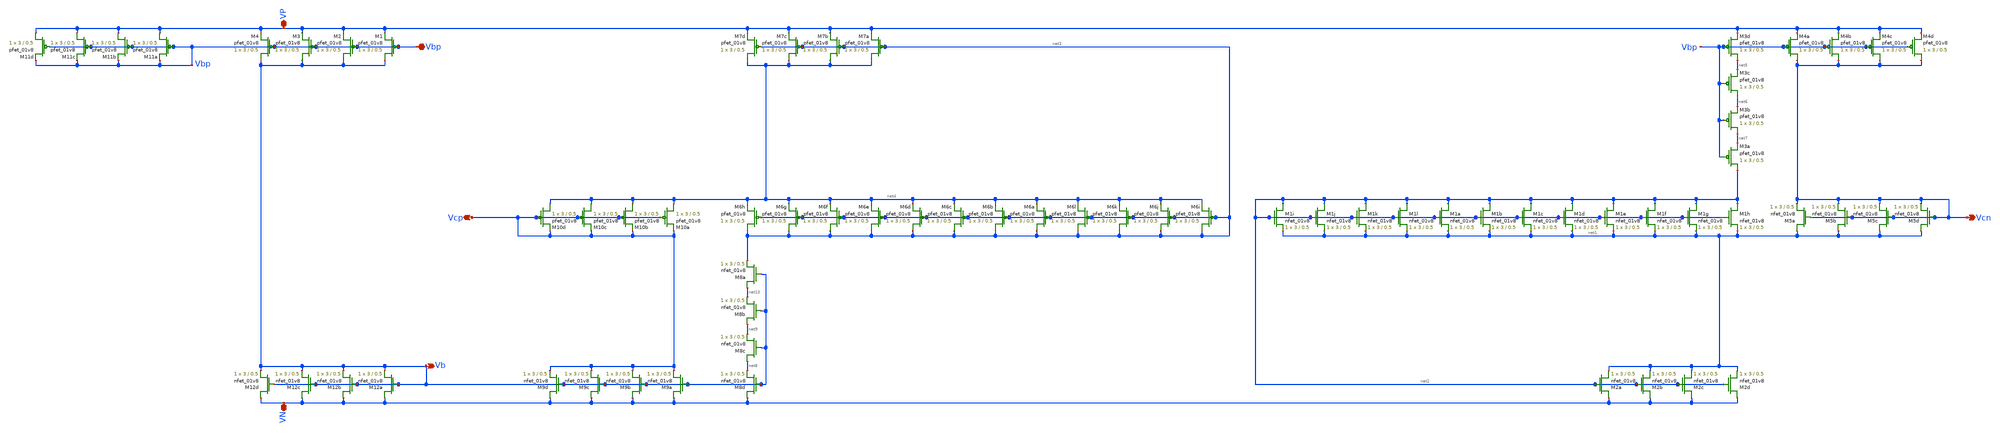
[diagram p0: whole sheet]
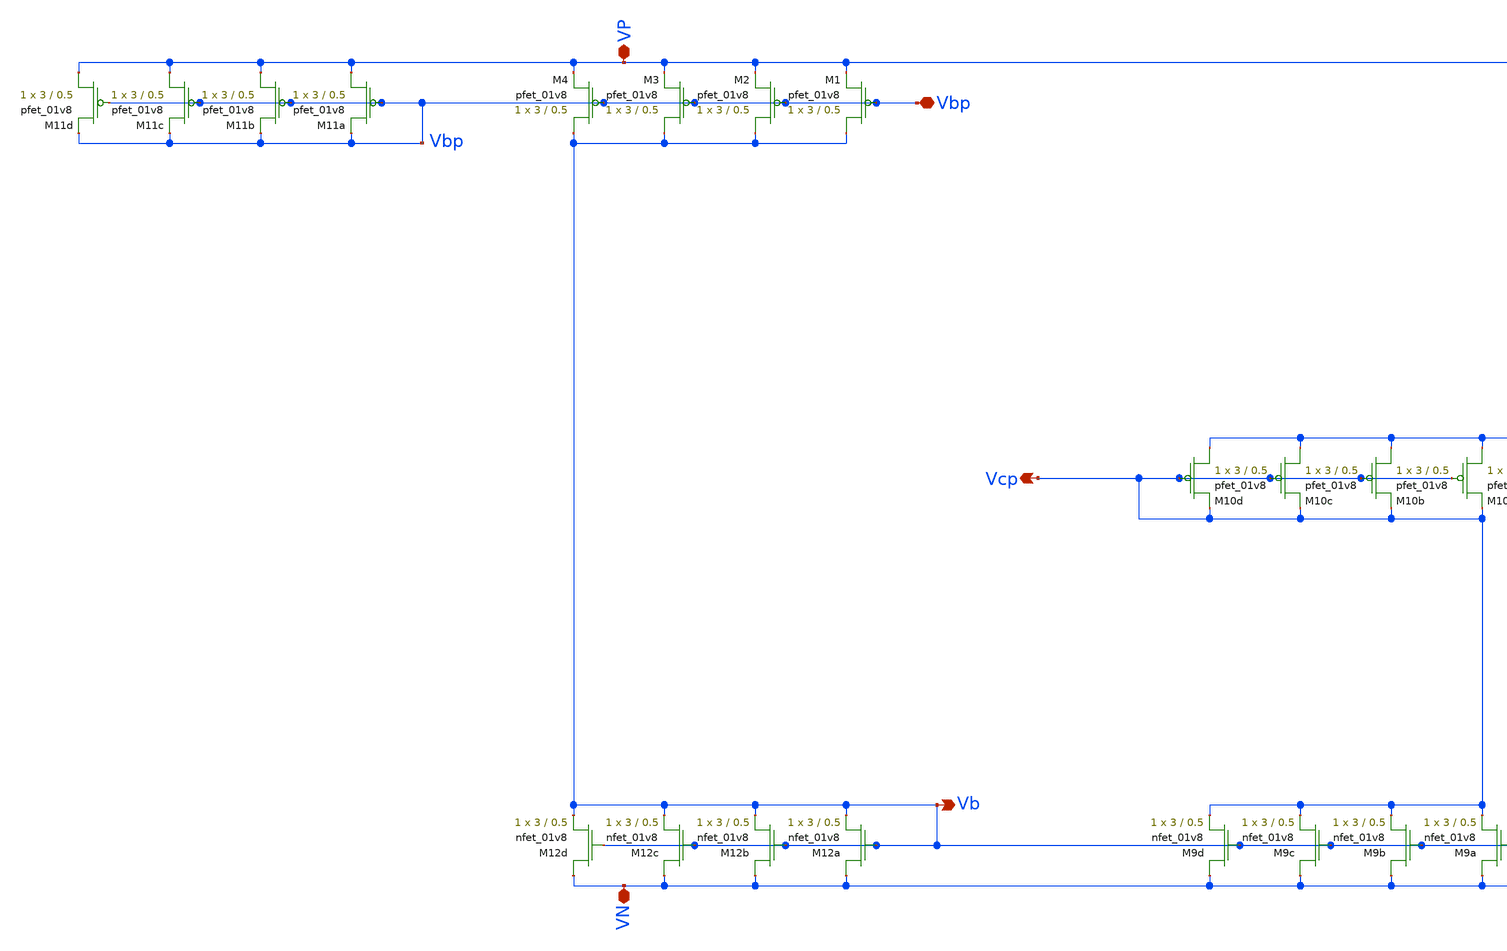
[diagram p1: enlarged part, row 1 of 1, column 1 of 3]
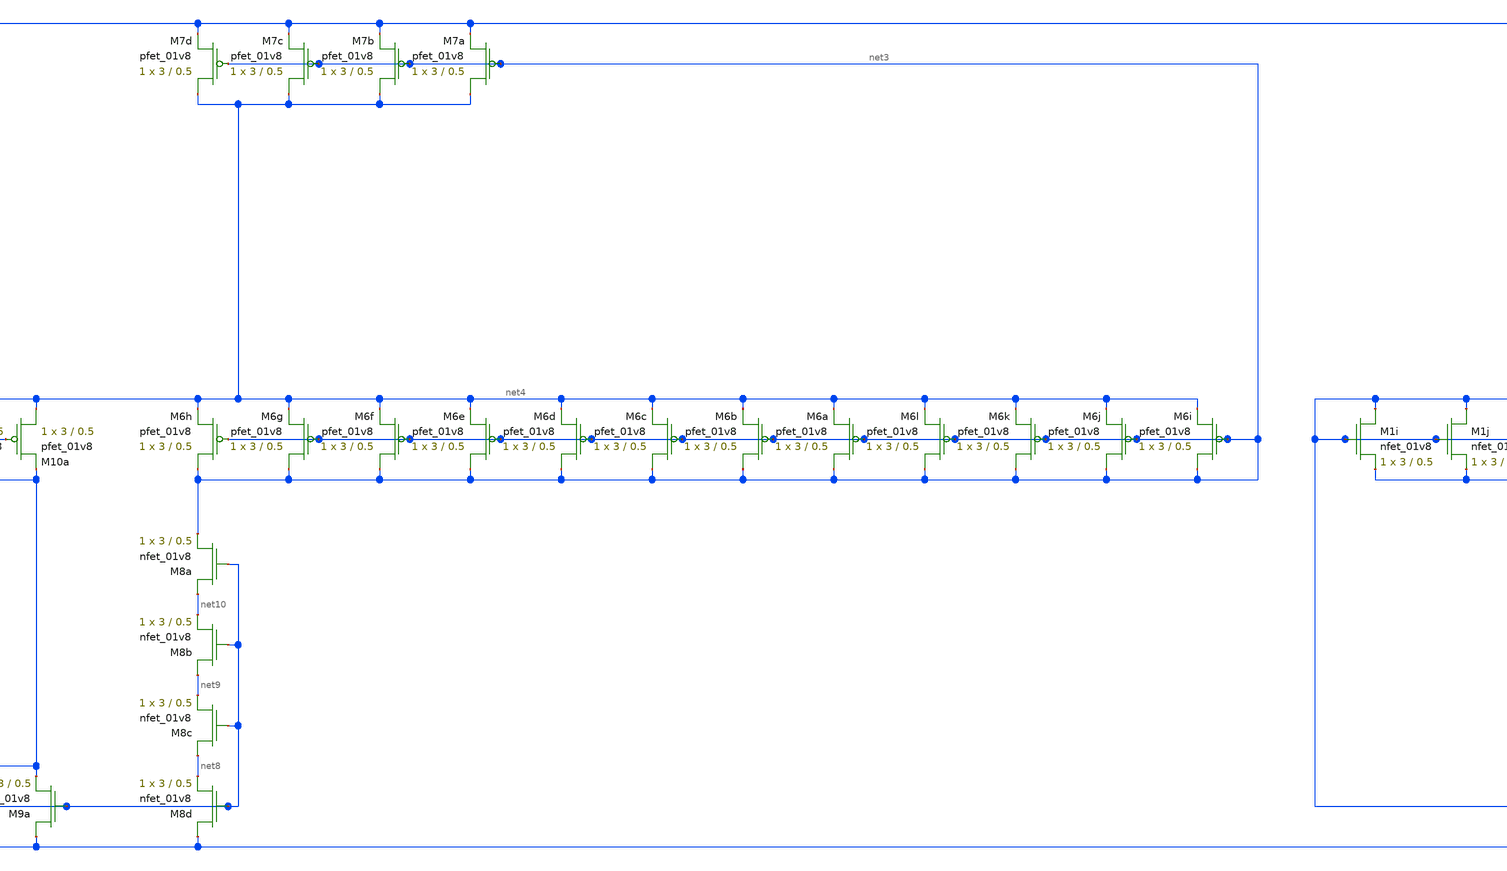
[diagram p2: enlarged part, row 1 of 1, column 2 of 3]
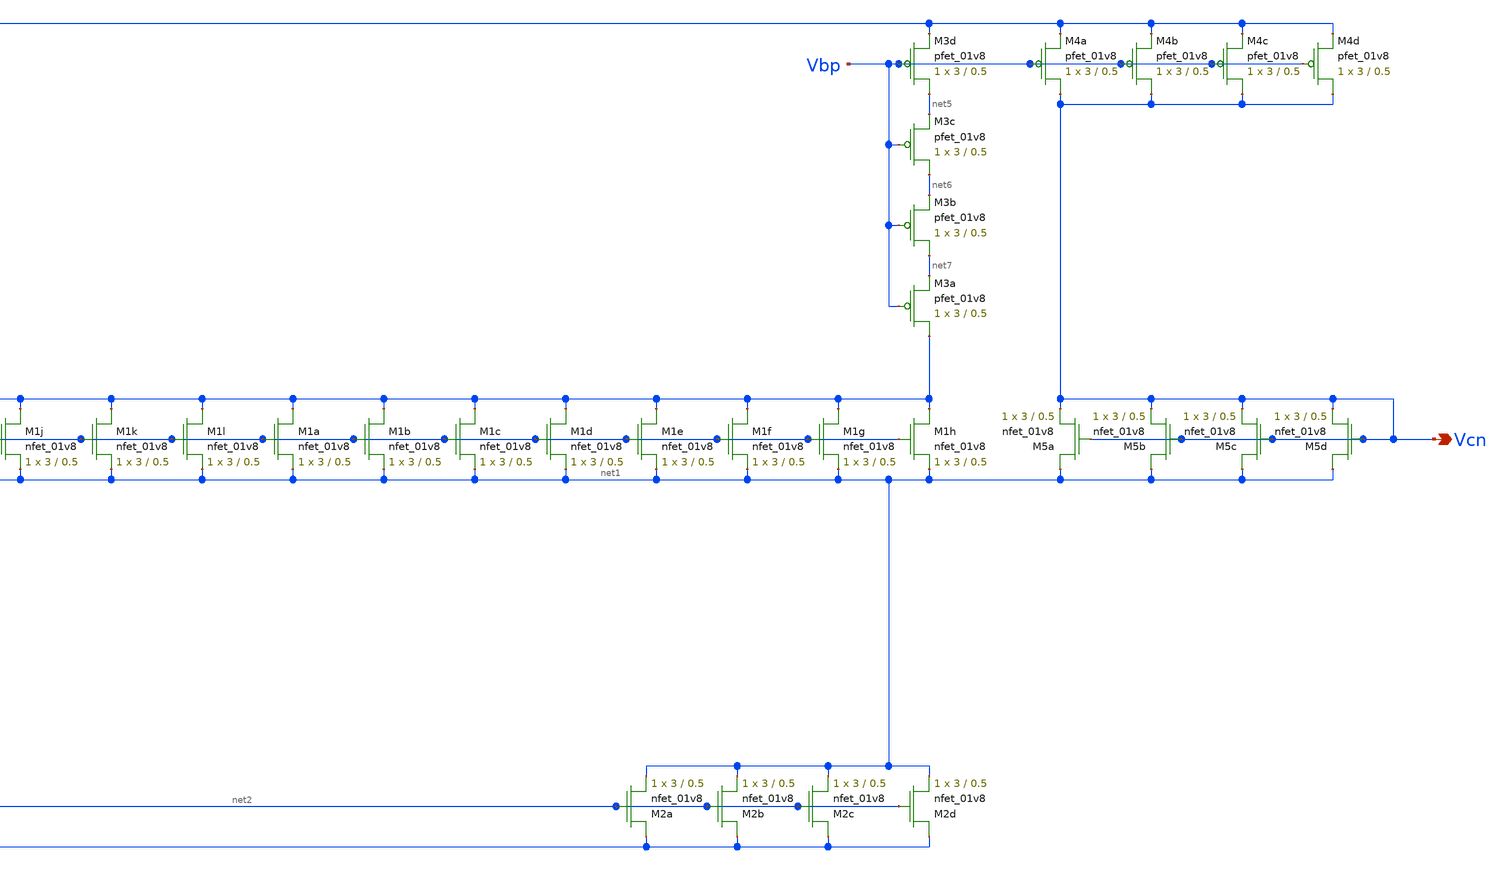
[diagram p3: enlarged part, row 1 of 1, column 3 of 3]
** sch_path: xschem/other_project_files/bias_schematic.sch
**.subckt bias_schematic VP VN Vcp Vbp Vcn Vb
*.iopin VP
*.iopin VN
*.opin Vcp
*.iopin Vbp
*.opin Vcn
*.opin Vb
XM1a net2 net2 net1 GND sky130_fd_pr__nfet_01v8 L=0.5 W=3 nf=1 ad='int((nf+1)/2) * W/nf * 0.29' as='int((nf+2)/2) * W/nf * 0.29'
+ pd='2*int((nf+1)/2) * (W/nf + 0.29)' ps='2*int((nf+2)/2) * (W/nf + 0.29)' nrd='0.29 / W' nrs='0.29 / W'
+ sa=0 sb=0 sd=0 mult=1 m=1
XM1b net2 net2 net1 GND sky130_fd_pr__nfet_01v8 L=0.5 W=3 nf=1 ad='int((nf+1)/2) * W/nf * 0.29' as='int((nf+2)/2) * W/nf * 0.29'
+ pd='2*int((nf+1)/2) * (W/nf + 0.29)' ps='2*int((nf+2)/2) * (W/nf + 0.29)' nrd='0.29 / W' nrs='0.29 / W'
+ sa=0 sb=0 sd=0 mult=1 m=1
XM1c net2 net2 net1 GND sky130_fd_pr__nfet_01v8 L=0.5 W=3 nf=1 ad='int((nf+1)/2) * W/nf * 0.29' as='int((nf+2)/2) * W/nf * 0.29'
+ pd='2*int((nf+1)/2) * (W/nf + 0.29)' ps='2*int((nf+2)/2) * (W/nf + 0.29)' nrd='0.29 / W' nrs='0.29 / W'
+ sa=0 sb=0 sd=0 mult=1 m=1
XM1d net2 net2 net1 GND sky130_fd_pr__nfet_01v8 L=0.5 W=3 nf=1 ad='int((nf+1)/2) * W/nf * 0.29' as='int((nf+2)/2) * W/nf * 0.29'
+ pd='2*int((nf+1)/2) * (W/nf + 0.29)' ps='2*int((nf+2)/2) * (W/nf + 0.29)' nrd='0.29 / W' nrs='0.29 / W'
+ sa=0 sb=0 sd=0 mult=1 m=1
XM2a VN net2 net1 GND sky130_fd_pr__nfet_01v8 L=0.5 W=3 nf=1 ad='int((nf+1)/2) * W/nf * 0.29' as='int((nf+2)/2) * W/nf * 0.29'
+ pd='2*int((nf+1)/2) * (W/nf + 0.29)' ps='2*int((nf+2)/2) * (W/nf + 0.29)' nrd='0.29 / W' nrs='0.29 / W'
+ sa=0 sb=0 sd=0 mult=1 m=1
XM2b VN net2 net1 GND sky130_fd_pr__nfet_01v8 L=0.5 W=3 nf=1 ad='int((nf+1)/2) * W/nf * 0.29' as='int((nf+2)/2) * W/nf * 0.29'
+ pd='2*int((nf+1)/2) * (W/nf + 0.29)' ps='2*int((nf+2)/2) * (W/nf + 0.29)' nrd='0.29 / W' nrs='0.29 / W'
+ sa=0 sb=0 sd=0 mult=1 m=1
XM2c VN net2 net1 GND sky130_fd_pr__nfet_01v8 L=0.5 W=3 nf=1 ad='int((nf+1)/2) * W/nf * 0.29' as='int((nf+2)/2) * W/nf * 0.29'
+ pd='2*int((nf+1)/2) * (W/nf + 0.29)' ps='2*int((nf+2)/2) * (W/nf + 0.29)' nrd='0.29 / W' nrs='0.29 / W'
+ sa=0 sb=0 sd=0 mult=1 m=1
XM2d VN net2 net1 GND sky130_fd_pr__nfet_01v8 L=0.5 W=3 nf=1 ad='int((nf+1)/2) * W/nf * 0.29' as='int((nf+2)/2) * W/nf * 0.29'
+ pd='2*int((nf+1)/2) * (W/nf + 0.29)' ps='2*int((nf+2)/2) * (W/nf + 0.29)' nrd='0.29 / W' nrs='0.29 / W'
+ sa=0 sb=0 sd=0 mult=1 m=1
XM3a net2 Vbp net7 VDD sky130_fd_pr__pfet_01v8 L=0.5 W=3 nf=1 ad='int((nf+1)/2) * W/nf * 0.29' as='int((nf+2)/2) * W/nf * 0.29'
+ pd='2*int((nf+1)/2) * (W/nf + 0.29)' ps='2*int((nf+2)/2) * (W/nf + 0.29)' nrd='0.29 / W' nrs='0.29 / W'
+ sa=0 sb=0 sd=0 mult=1 m=1
XM3b net7 Vbp net6 VDD sky130_fd_pr__pfet_01v8 L=0.5 W=3 nf=1 ad='int((nf+1)/2) * W/nf * 0.29' as='int((nf+2)/2) * W/nf * 0.29'
+ pd='2*int((nf+1)/2) * (W/nf + 0.29)' ps='2*int((nf+2)/2) * (W/nf + 0.29)' nrd='0.29 / W' nrs='0.29 / W'
+ sa=0 sb=0 sd=0 mult=1 m=1
XM3c net6 Vbp net5 VDD sky130_fd_pr__pfet_01v8 L=0.5 W=3 nf=1 ad='int((nf+1)/2) * W/nf * 0.29' as='int((nf+2)/2) * W/nf * 0.29'
+ pd='2*int((nf+1)/2) * (W/nf + 0.29)' ps='2*int((nf+2)/2) * (W/nf + 0.29)' nrd='0.29 / W' nrs='0.29 / W'
+ sa=0 sb=0 sd=0 mult=1 m=1
XM3d net5 Vbp VP VDD sky130_fd_pr__pfet_01v8 L=0.5 W=3 nf=1 ad='int((nf+1)/2) * W/nf * 0.29' as='int((nf+2)/2) * W/nf * 0.29'
+ pd='2*int((nf+1)/2) * (W/nf + 0.29)' ps='2*int((nf+2)/2) * (W/nf + 0.29)' nrd='0.29 / W' nrs='0.29 / W'
+ sa=0 sb=0 sd=0 mult=1 m=1
XM4a Vcn Vbp VP VDD sky130_fd_pr__pfet_01v8 L=0.5 W=3 nf=1 ad='int((nf+1)/2) * W/nf * 0.29' as='int((nf+2)/2) * W/nf * 0.29'
+ pd='2*int((nf+1)/2) * (W/nf + 0.29)' ps='2*int((nf+2)/2) * (W/nf + 0.29)' nrd='0.29 / W' nrs='0.29 / W'
+ sa=0 sb=0 sd=0 mult=1 m=1
XM4b Vcn Vbp VP VDD sky130_fd_pr__pfet_01v8 L=0.5 W=3 nf=1 ad='int((nf+1)/2) * W/nf * 0.29' as='int((nf+2)/2) * W/nf * 0.29'
+ pd='2*int((nf+1)/2) * (W/nf + 0.29)' ps='2*int((nf+2)/2) * (W/nf + 0.29)' nrd='0.29 / W' nrs='0.29 / W'
+ sa=0 sb=0 sd=0 mult=1 m=1
XM4c Vcn Vbp VP VDD sky130_fd_pr__pfet_01v8 L=0.5 W=3 nf=1 ad='int((nf+1)/2) * W/nf * 0.29' as='int((nf+2)/2) * W/nf * 0.29'
+ pd='2*int((nf+1)/2) * (W/nf + 0.29)' ps='2*int((nf+2)/2) * (W/nf + 0.29)' nrd='0.29 / W' nrs='0.29 / W'
+ sa=0 sb=0 sd=0 mult=1 m=1
XM4d Vcn Vbp VP VDD sky130_fd_pr__pfet_01v8 L=0.5 W=3 nf=1 ad='int((nf+1)/2) * W/nf * 0.29' as='int((nf+2)/2) * W/nf * 0.29'
+ pd='2*int((nf+1)/2) * (W/nf + 0.29)' ps='2*int((nf+2)/2) * (W/nf + 0.29)' nrd='0.29 / W' nrs='0.29 / W'
+ sa=0 sb=0 sd=0 mult=1 m=1
XM11a VP Vbp Vbp VDD sky130_fd_pr__pfet_01v8 L=0.5 W=3 nf=1 ad='int((nf+1)/2) * W/nf * 0.29' as='int((nf+2)/2) * W/nf * 0.29'
+ pd='2*int((nf+1)/2) * (W/nf + 0.29)' ps='2*int((nf+2)/2) * (W/nf + 0.29)' nrd='0.29 / W' nrs='0.29 / W'
+ sa=0 sb=0 sd=0 mult=1 m=1
XM11b VP Vbp Vbp VDD sky130_fd_pr__pfet_01v8 L=0.5 W=3 nf=1 ad='int((nf+1)/2) * W/nf * 0.29' as='int((nf+2)/2) * W/nf * 0.29'
+ pd='2*int((nf+1)/2) * (W/nf + 0.29)' ps='2*int((nf+2)/2) * (W/nf + 0.29)' nrd='0.29 / W' nrs='0.29 / W'
+ sa=0 sb=0 sd=0 mult=1 m=1
XM11c VP Vbp Vbp VDD sky130_fd_pr__pfet_01v8 L=0.5 W=3 nf=1 ad='int((nf+1)/2) * W/nf * 0.29' as='int((nf+2)/2) * W/nf * 0.29'
+ pd='2*int((nf+1)/2) * (W/nf + 0.29)' ps='2*int((nf+2)/2) * (W/nf + 0.29)' nrd='0.29 / W' nrs='0.29 / W'
+ sa=0 sb=0 sd=0 mult=1 m=1
XM11d VP Vbp Vbp VDD sky130_fd_pr__pfet_01v8 L=0.5 W=3 nf=1 ad='int((nf+1)/2) * W/nf * 0.29' as='int((nf+2)/2) * W/nf * 0.29'
+ pd='2*int((nf+1)/2) * (W/nf + 0.29)' ps='2*int((nf+2)/2) * (W/nf + 0.29)' nrd='0.29 / W' nrs='0.29 / W'
+ sa=0 sb=0 sd=0 mult=1 m=1
XM5a net1 Vcn Vcn GND sky130_fd_pr__nfet_01v8 L=0.5 W=3 nf=1 ad='int((nf+1)/2) * W/nf * 0.29' as='int((nf+2)/2) * W/nf * 0.29'
+ pd='2*int((nf+1)/2) * (W/nf + 0.29)' ps='2*int((nf+2)/2) * (W/nf + 0.29)' nrd='0.29 / W' nrs='0.29 / W'
+ sa=0 sb=0 sd=0 mult=1 m=1
XM5b net1 Vcn Vcn GND sky130_fd_pr__nfet_01v8 L=0.5 W=3 nf=1 ad='int((nf+1)/2) * W/nf * 0.29' as='int((nf+2)/2) * W/nf * 0.29'
+ pd='2*int((nf+1)/2) * (W/nf + 0.29)' ps='2*int((nf+2)/2) * (W/nf + 0.29)' nrd='0.29 / W' nrs='0.29 / W'
+ sa=0 sb=0 sd=0 mult=1 m=1
XM5c net1 Vcn Vcn GND sky130_fd_pr__nfet_01v8 L=0.5 W=3 nf=1 ad='int((nf+1)/2) * W/nf * 0.29' as='int((nf+2)/2) * W/nf * 0.29'
+ pd='2*int((nf+1)/2) * (W/nf + 0.29)' ps='2*int((nf+2)/2) * (W/nf + 0.29)' nrd='0.29 / W' nrs='0.29 / W'
+ sa=0 sb=0 sd=0 mult=1 m=1
XM5d net1 Vcn Vcn GND sky130_fd_pr__nfet_01v8 L=0.5 W=3 nf=1 ad='int((nf+1)/2) * W/nf * 0.29' as='int((nf+2)/2) * W/nf * 0.29'
+ pd='2*int((nf+1)/2) * (W/nf + 0.29)' ps='2*int((nf+2)/2) * (W/nf + 0.29)' nrd='0.29 / W' nrs='0.29 / W'
+ sa=0 sb=0 sd=0 mult=1 m=1
XM8a net10 Vb net3 GND sky130_fd_pr__nfet_01v8 L=0.5 W=3 nf=1 ad='int((nf+1)/2) * W/nf * 0.29' as='int((nf+2)/2) * W/nf * 0.29'
+ pd='2*int((nf+1)/2) * (W/nf + 0.29)' ps='2*int((nf+2)/2) * (W/nf + 0.29)' nrd='0.29 / W' nrs='0.29 / W'
+ sa=0 sb=0 sd=0 mult=1 m=1
XM8b net9 Vb net10 GND sky130_fd_pr__nfet_01v8 L=0.5 W=3 nf=1 ad='int((nf+1)/2) * W/nf * 0.29' as='int((nf+2)/2) * W/nf * 0.29'
+ pd='2*int((nf+1)/2) * (W/nf + 0.29)' ps='2*int((nf+2)/2) * (W/nf + 0.29)' nrd='0.29 / W' nrs='0.29 / W'
+ sa=0 sb=0 sd=0 mult=1 m=1
XM8c net8 Vb net9 GND sky130_fd_pr__nfet_01v8 L=0.5 W=3 nf=1 ad='int((nf+1)/2) * W/nf * 0.29' as='int((nf+2)/2) * W/nf * 0.29'
+ pd='2*int((nf+1)/2) * (W/nf + 0.29)' ps='2*int((nf+2)/2) * (W/nf + 0.29)' nrd='0.29 / W' nrs='0.29 / W'
+ sa=0 sb=0 sd=0 mult=1 m=1
XM8d VN Vb net8 GND sky130_fd_pr__nfet_01v8 L=0.5 W=3 nf=1 ad='int((nf+1)/2) * W/nf * 0.29' as='int((nf+2)/2) * W/nf * 0.29'
+ pd='2*int((nf+1)/2) * (W/nf + 0.29)' ps='2*int((nf+2)/2) * (W/nf + 0.29)' nrd='0.29 / W' nrs='0.29 / W'
+ sa=0 sb=0 sd=0 mult=1 m=1
XM6a net3 net3 net4 VDD sky130_fd_pr__pfet_01v8 L=0.5 W=3 nf=1 ad='int((nf+1)/2) * W/nf * 0.29' as='int((nf+2)/2) * W/nf * 0.29'
+ pd='2*int((nf+1)/2) * (W/nf + 0.29)' ps='2*int((nf+2)/2) * (W/nf + 0.29)' nrd='0.29 / W' nrs='0.29 / W'
+ sa=0 sb=0 sd=0 mult=1 m=1
XM6b net3 net3 net4 VDD sky130_fd_pr__pfet_01v8 L=0.5 W=3 nf=1 ad='int((nf+1)/2) * W/nf * 0.29' as='int((nf+2)/2) * W/nf * 0.29'
+ pd='2*int((nf+1)/2) * (W/nf + 0.29)' ps='2*int((nf+2)/2) * (W/nf + 0.29)' nrd='0.29 / W' nrs='0.29 / W'
+ sa=0 sb=0 sd=0 mult=1 m=1
XM6c net3 net3 net4 VDD sky130_fd_pr__pfet_01v8 L=0.5 W=3 nf=1 ad='int((nf+1)/2) * W/nf * 0.29' as='int((nf+2)/2) * W/nf * 0.29'
+ pd='2*int((nf+1)/2) * (W/nf + 0.29)' ps='2*int((nf+2)/2) * (W/nf + 0.29)' nrd='0.29 / W' nrs='0.29 / W'
+ sa=0 sb=0 sd=0 mult=1 m=1
XM6d net3 net3 net4 VDD sky130_fd_pr__pfet_01v8 L=0.5 W=3 nf=1 ad='int((nf+1)/2) * W/nf * 0.29' as='int((nf+2)/2) * W/nf * 0.29'
+ pd='2*int((nf+1)/2) * (W/nf + 0.29)' ps='2*int((nf+2)/2) * (W/nf + 0.29)' nrd='0.29 / W' nrs='0.29 / W'
+ sa=0 sb=0 sd=0 mult=1 m=1
XM7a net4 net3 VP VDD sky130_fd_pr__pfet_01v8 L=0.5 W=3 nf=1 ad='int((nf+1)/2) * W/nf * 0.29' as='int((nf+2)/2) * W/nf * 0.29'
+ pd='2*int((nf+1)/2) * (W/nf + 0.29)' ps='2*int((nf+2)/2) * (W/nf + 0.29)' nrd='0.29 / W' nrs='0.29 / W'
+ sa=0 sb=0 sd=0 mult=1 m=1
XM7b net4 net3 VP VDD sky130_fd_pr__pfet_01v8 L=0.5 W=3 nf=1 ad='int((nf+1)/2) * W/nf * 0.29' as='int((nf+2)/2) * W/nf * 0.29'
+ pd='2*int((nf+1)/2) * (W/nf + 0.29)' ps='2*int((nf+2)/2) * (W/nf + 0.29)' nrd='0.29 / W' nrs='0.29 / W'
+ sa=0 sb=0 sd=0 mult=1 m=1
XM7c net4 net3 VP VDD sky130_fd_pr__pfet_01v8 L=0.5 W=3 nf=1 ad='int((nf+1)/2) * W/nf * 0.29' as='int((nf+2)/2) * W/nf * 0.29'
+ pd='2*int((nf+1)/2) * (W/nf + 0.29)' ps='2*int((nf+2)/2) * (W/nf + 0.29)' nrd='0.29 / W' nrs='0.29 / W'
+ sa=0 sb=0 sd=0 mult=1 m=1
XM7d net4 net3 VP VDD sky130_fd_pr__pfet_01v8 L=0.5 W=3 nf=1 ad='int((nf+1)/2) * W/nf * 0.29' as='int((nf+2)/2) * W/nf * 0.29'
+ pd='2*int((nf+1)/2) * (W/nf + 0.29)' ps='2*int((nf+2)/2) * (W/nf + 0.29)' nrd='0.29 / W' nrs='0.29 / W'
+ sa=0 sb=0 sd=0 mult=1 m=1
XM10d net4 Vcp Vcp VDD sky130_fd_pr__pfet_01v8 L=0.5 W=3 nf=1 ad='int((nf+1)/2) * W/nf * 0.29' as='int((nf+2)/2) * W/nf * 0.29'
+ pd='2*int((nf+1)/2) * (W/nf + 0.29)' ps='2*int((nf+2)/2) * (W/nf + 0.29)' nrd='0.29 / W' nrs='0.29 / W'
+ sa=0 sb=0 sd=0 mult=1 m=1
XM10c net4 Vcp Vcp VDD sky130_fd_pr__pfet_01v8 L=0.5 W=3 nf=1 ad='int((nf+1)/2) * W/nf * 0.29' as='int((nf+2)/2) * W/nf * 0.29'
+ pd='2*int((nf+1)/2) * (W/nf + 0.29)' ps='2*int((nf+2)/2) * (W/nf + 0.29)' nrd='0.29 / W' nrs='0.29 / W'
+ sa=0 sb=0 sd=0 mult=1 m=1
XM10b net4 Vcp Vcp VDD sky130_fd_pr__pfet_01v8 L=0.5 W=3 nf=1 ad='int((nf+1)/2) * W/nf * 0.29' as='int((nf+2)/2) * W/nf * 0.29'
+ pd='2*int((nf+1)/2) * (W/nf + 0.29)' ps='2*int((nf+2)/2) * (W/nf + 0.29)' nrd='0.29 / W' nrs='0.29 / W'
+ sa=0 sb=0 sd=0 mult=1 m=1
XM10a net4 Vcp Vcp VDD sky130_fd_pr__pfet_01v8 L=0.5 W=3 nf=1 ad='int((nf+1)/2) * W/nf * 0.29' as='int((nf+2)/2) * W/nf * 0.29'
+ pd='2*int((nf+1)/2) * (W/nf + 0.29)' ps='2*int((nf+2)/2) * (W/nf + 0.29)' nrd='0.29 / W' nrs='0.29 / W'
+ sa=0 sb=0 sd=0 mult=1 m=1
XM9a VN Vb Vcp GND sky130_fd_pr__nfet_01v8 L=0.5 W=3 nf=1 ad='int((nf+1)/2) * W/nf * 0.29' as='int((nf+2)/2) * W/nf * 0.29'
+ pd='2*int((nf+1)/2) * (W/nf + 0.29)' ps='2*int((nf+2)/2) * (W/nf + 0.29)' nrd='0.29 / W' nrs='0.29 / W'
+ sa=0 sb=0 sd=0 mult=1 m=1
XM9b VN Vb Vcp GND sky130_fd_pr__nfet_01v8 L=0.5 W=3 nf=1 ad='int((nf+1)/2) * W/nf * 0.29' as='int((nf+2)/2) * W/nf * 0.29'
+ pd='2*int((nf+1)/2) * (W/nf + 0.29)' ps='2*int((nf+2)/2) * (W/nf + 0.29)' nrd='0.29 / W' nrs='0.29 / W'
+ sa=0 sb=0 sd=0 mult=1 m=1
XM9c VN Vb Vcp GND sky130_fd_pr__nfet_01v8 L=0.5 W=3 nf=1 ad='int((nf+1)/2) * W/nf * 0.29' as='int((nf+2)/2) * W/nf * 0.29'
+ pd='2*int((nf+1)/2) * (W/nf + 0.29)' ps='2*int((nf+2)/2) * (W/nf + 0.29)' nrd='0.29 / W' nrs='0.29 / W'
+ sa=0 sb=0 sd=0 mult=1 m=1
XM9d VN Vb Vcp GND sky130_fd_pr__nfet_01v8 L=0.5 W=3 nf=1 ad='int((nf+1)/2) * W/nf * 0.29' as='int((nf+2)/2) * W/nf * 0.29'
+ pd='2*int((nf+1)/2) * (W/nf + 0.29)' ps='2*int((nf+2)/2) * (W/nf + 0.29)' nrd='0.29 / W' nrs='0.29 / W'
+ sa=0 sb=0 sd=0 mult=1 m=1
XM12a VN Vb Vb GND sky130_fd_pr__nfet_01v8 L=0.5 W=3 nf=1 ad='int((nf+1)/2) * W/nf * 0.29' as='int((nf+2)/2) * W/nf * 0.29'
+ pd='2*int((nf+1)/2) * (W/nf + 0.29)' ps='2*int((nf+2)/2) * (W/nf + 0.29)' nrd='0.29 / W' nrs='0.29 / W'
+ sa=0 sb=0 sd=0 mult=1 m=1
XM12b VN Vb Vb GND sky130_fd_pr__nfet_01v8 L=0.5 W=3 nf=1 ad='int((nf+1)/2) * W/nf * 0.29' as='int((nf+2)/2) * W/nf * 0.29'
+ pd='2*int((nf+1)/2) * (W/nf + 0.29)' ps='2*int((nf+2)/2) * (W/nf + 0.29)' nrd='0.29 / W' nrs='0.29 / W'
+ sa=0 sb=0 sd=0 mult=1 m=1
XM12c VN Vb Vb GND sky130_fd_pr__nfet_01v8 L=0.5 W=3 nf=1 ad='int((nf+1)/2) * W/nf * 0.29' as='int((nf+2)/2) * W/nf * 0.29'
+ pd='2*int((nf+1)/2) * (W/nf + 0.29)' ps='2*int((nf+2)/2) * (W/nf + 0.29)' nrd='0.29 / W' nrs='0.29 / W'
+ sa=0 sb=0 sd=0 mult=1 m=1
XM12d VN Vb Vb GND sky130_fd_pr__nfet_01v8 L=0.5 W=3 nf=1 ad='int((nf+1)/2) * W/nf * 0.29' as='int((nf+2)/2) * W/nf * 0.29'
+ pd='2*int((nf+1)/2) * (W/nf + 0.29)' ps='2*int((nf+2)/2) * (W/nf + 0.29)' nrd='0.29 / W' nrs='0.29 / W'
+ sa=0 sb=0 sd=0 mult=1 m=1
XM1 Vb Vbp VP VDD sky130_fd_pr__pfet_01v8 L=0.5 W=3 nf=1 ad='int((nf+1)/2) * W/nf * 0.29' as='int((nf+2)/2) * W/nf * 0.29'
+ pd='2*int((nf+1)/2) * (W/nf + 0.29)' ps='2*int((nf+2)/2) * (W/nf + 0.29)' nrd='0.29 / W' nrs='0.29 / W'
+ sa=0 sb=0 sd=0 mult=1 m=1
XM2 Vb Vbp VP VDD sky130_fd_pr__pfet_01v8 L=0.5 W=3 nf=1 ad='int((nf+1)/2) * W/nf * 0.29' as='int((nf+2)/2) * W/nf * 0.29'
+ pd='2*int((nf+1)/2) * (W/nf + 0.29)' ps='2*int((nf+2)/2) * (W/nf + 0.29)' nrd='0.29 / W' nrs='0.29 / W'
+ sa=0 sb=0 sd=0 mult=1 m=1
XM3 Vb Vbp VP VDD sky130_fd_pr__pfet_01v8 L=0.5 W=3 nf=1 ad='int((nf+1)/2) * W/nf * 0.29' as='int((nf+2)/2) * W/nf * 0.29'
+ pd='2*int((nf+1)/2) * (W/nf + 0.29)' ps='2*int((nf+2)/2) * (W/nf + 0.29)' nrd='0.29 / W' nrs='0.29 / W'
+ sa=0 sb=0 sd=0 mult=1 m=1
XM4 Vb Vbp VP VDD sky130_fd_pr__pfet_01v8 L=0.5 W=3 nf=1 ad='int((nf+1)/2) * W/nf * 0.29' as='int((nf+2)/2) * W/nf * 0.29'
+ pd='2*int((nf+1)/2) * (W/nf + 0.29)' ps='2*int((nf+2)/2) * (W/nf + 0.29)' nrd='0.29 / W' nrs='0.29 / W'
+ sa=0 sb=0 sd=0 mult=1 m=1
XM1e net2 net2 net1 GND sky130_fd_pr__nfet_01v8 L=0.5 W=3 nf=1 ad='int((nf+1)/2) * W/nf * 0.29' as='int((nf+2)/2) * W/nf * 0.29'
+ pd='2*int((nf+1)/2) * (W/nf + 0.29)' ps='2*int((nf+2)/2) * (W/nf + 0.29)' nrd='0.29 / W' nrs='0.29 / W'
+ sa=0 sb=0 sd=0 mult=1 m=1
XM1f net2 net2 net1 GND sky130_fd_pr__nfet_01v8 L=0.5 W=3 nf=1 ad='int((nf+1)/2) * W/nf * 0.29' as='int((nf+2)/2) * W/nf * 0.29'
+ pd='2*int((nf+1)/2) * (W/nf + 0.29)' ps='2*int((nf+2)/2) * (W/nf + 0.29)' nrd='0.29 / W' nrs='0.29 / W'
+ sa=0 sb=0 sd=0 mult=1 m=1
XM1g net2 net2 net1 GND sky130_fd_pr__nfet_01v8 L=0.5 W=3 nf=1 ad='int((nf+1)/2) * W/nf * 0.29' as='int((nf+2)/2) * W/nf * 0.29'
+ pd='2*int((nf+1)/2) * (W/nf + 0.29)' ps='2*int((nf+2)/2) * (W/nf + 0.29)' nrd='0.29 / W' nrs='0.29 / W'
+ sa=0 sb=0 sd=0 mult=1 m=1
XM1h net2 net2 net1 GND sky130_fd_pr__nfet_01v8 L=0.5 W=3 nf=1 ad='int((nf+1)/2) * W/nf * 0.29' as='int((nf+2)/2) * W/nf * 0.29'
+ pd='2*int((nf+1)/2) * (W/nf + 0.29)' ps='2*int((nf+2)/2) * (W/nf + 0.29)' nrd='0.29 / W' nrs='0.29 / W'
+ sa=0 sb=0 sd=0 mult=1 m=1
XM6e net3 net3 net4 VDD sky130_fd_pr__pfet_01v8 L=0.5 W=3 nf=1 ad='int((nf+1)/2) * W/nf * 0.29' as='int((nf+2)/2) * W/nf * 0.29'
+ pd='2*int((nf+1)/2) * (W/nf + 0.29)' ps='2*int((nf+2)/2) * (W/nf + 0.29)' nrd='0.29 / W' nrs='0.29 / W'
+ sa=0 sb=0 sd=0 mult=1 m=1
XM6f net3 net3 net4 VDD sky130_fd_pr__pfet_01v8 L=0.5 W=3 nf=1 ad='int((nf+1)/2) * W/nf * 0.29' as='int((nf+2)/2) * W/nf * 0.29'
+ pd='2*int((nf+1)/2) * (W/nf + 0.29)' ps='2*int((nf+2)/2) * (W/nf + 0.29)' nrd='0.29 / W' nrs='0.29 / W'
+ sa=0 sb=0 sd=0 mult=1 m=1
XM6g net3 net3 net4 VDD sky130_fd_pr__pfet_01v8 L=0.5 W=3 nf=1 ad='int((nf+1)/2) * W/nf * 0.29' as='int((nf+2)/2) * W/nf * 0.29'
+ pd='2*int((nf+1)/2) * (W/nf + 0.29)' ps='2*int((nf+2)/2) * (W/nf + 0.29)' nrd='0.29 / W' nrs='0.29 / W'
+ sa=0 sb=0 sd=0 mult=1 m=1
XM6h net3 net3 net4 VDD sky130_fd_pr__pfet_01v8 L=0.5 W=3 nf=1 ad='int((nf+1)/2) * W/nf * 0.29' as='int((nf+2)/2) * W/nf * 0.29'
+ pd='2*int((nf+1)/2) * (W/nf + 0.29)' ps='2*int((nf+2)/2) * (W/nf + 0.29)' nrd='0.29 / W' nrs='0.29 / W'
+ sa=0 sb=0 sd=0 mult=1 m=1
XM1i net2 net2 net1 GND sky130_fd_pr__nfet_01v8 L=0.5 W=3 nf=1 ad='int((nf+1)/2) * W/nf * 0.29' as='int((nf+2)/2) * W/nf * 0.29'
+ pd='2*int((nf+1)/2) * (W/nf + 0.29)' ps='2*int((nf+2)/2) * (W/nf + 0.29)' nrd='0.29 / W' nrs='0.29 / W'
+ sa=0 sb=0 sd=0 mult=1 m=1
XM1j net2 net2 net1 GND sky130_fd_pr__nfet_01v8 L=0.5 W=3 nf=1 ad='int((nf+1)/2) * W/nf * 0.29' as='int((nf+2)/2) * W/nf * 0.29'
+ pd='2*int((nf+1)/2) * (W/nf + 0.29)' ps='2*int((nf+2)/2) * (W/nf + 0.29)' nrd='0.29 / W' nrs='0.29 / W'
+ sa=0 sb=0 sd=0 mult=1 m=1
XM1k net2 net2 net1 GND sky130_fd_pr__nfet_01v8 L=0.5 W=3 nf=1 ad='int((nf+1)/2) * W/nf * 0.29' as='int((nf+2)/2) * W/nf * 0.29'
+ pd='2*int((nf+1)/2) * (W/nf + 0.29)' ps='2*int((nf+2)/2) * (W/nf + 0.29)' nrd='0.29 / W' nrs='0.29 / W'
+ sa=0 sb=0 sd=0 mult=1 m=1
XM1l net2 net2 net1 GND sky130_fd_pr__nfet_01v8 L=0.5 W=3 nf=1 ad='int((nf+1)/2) * W/nf * 0.29' as='int((nf+2)/2) * W/nf * 0.29'
+ pd='2*int((nf+1)/2) * (W/nf + 0.29)' ps='2*int((nf+2)/2) * (W/nf + 0.29)' nrd='0.29 / W' nrs='0.29 / W'
+ sa=0 sb=0 sd=0 mult=1 m=1
XM6i net3 net3 net4 VDD sky130_fd_pr__pfet_01v8 L=0.5 W=3 nf=1 ad='int((nf+1)/2) * W/nf * 0.29' as='int((nf+2)/2) * W/nf * 0.29'
+ pd='2*int((nf+1)/2) * (W/nf + 0.29)' ps='2*int((nf+2)/2) * (W/nf + 0.29)' nrd='0.29 / W' nrs='0.29 / W'
+ sa=0 sb=0 sd=0 mult=1 m=1
XM6j net3 net3 net4 VDD sky130_fd_pr__pfet_01v8 L=0.5 W=3 nf=1 ad='int((nf+1)/2) * W/nf * 0.29' as='int((nf+2)/2) * W/nf * 0.29'
+ pd='2*int((nf+1)/2) * (W/nf + 0.29)' ps='2*int((nf+2)/2) * (W/nf + 0.29)' nrd='0.29 / W' nrs='0.29 / W'
+ sa=0 sb=0 sd=0 mult=1 m=1
XM6k net3 net3 net4 VDD sky130_fd_pr__pfet_01v8 L=0.5 W=3 nf=1 ad='int((nf+1)/2) * W/nf * 0.29' as='int((nf+2)/2) * W/nf * 0.29'
+ pd='2*int((nf+1)/2) * (W/nf + 0.29)' ps='2*int((nf+2)/2) * (W/nf + 0.29)' nrd='0.29 / W' nrs='0.29 / W'
+ sa=0 sb=0 sd=0 mult=1 m=1
XM6l net3 net3 net4 VDD sky130_fd_pr__pfet_01v8 L=0.5 W=3 nf=1 ad='int((nf+1)/2) * W/nf * 0.29' as='int((nf+2)/2) * W/nf * 0.29'
+ pd='2*int((nf+1)/2) * (W/nf + 0.29)' ps='2*int((nf+2)/2) * (W/nf + 0.29)' nrd='0.29 / W' nrs='0.29 / W'
+ sa=0 sb=0 sd=0 mult=1 m=1
**.ends
.end
